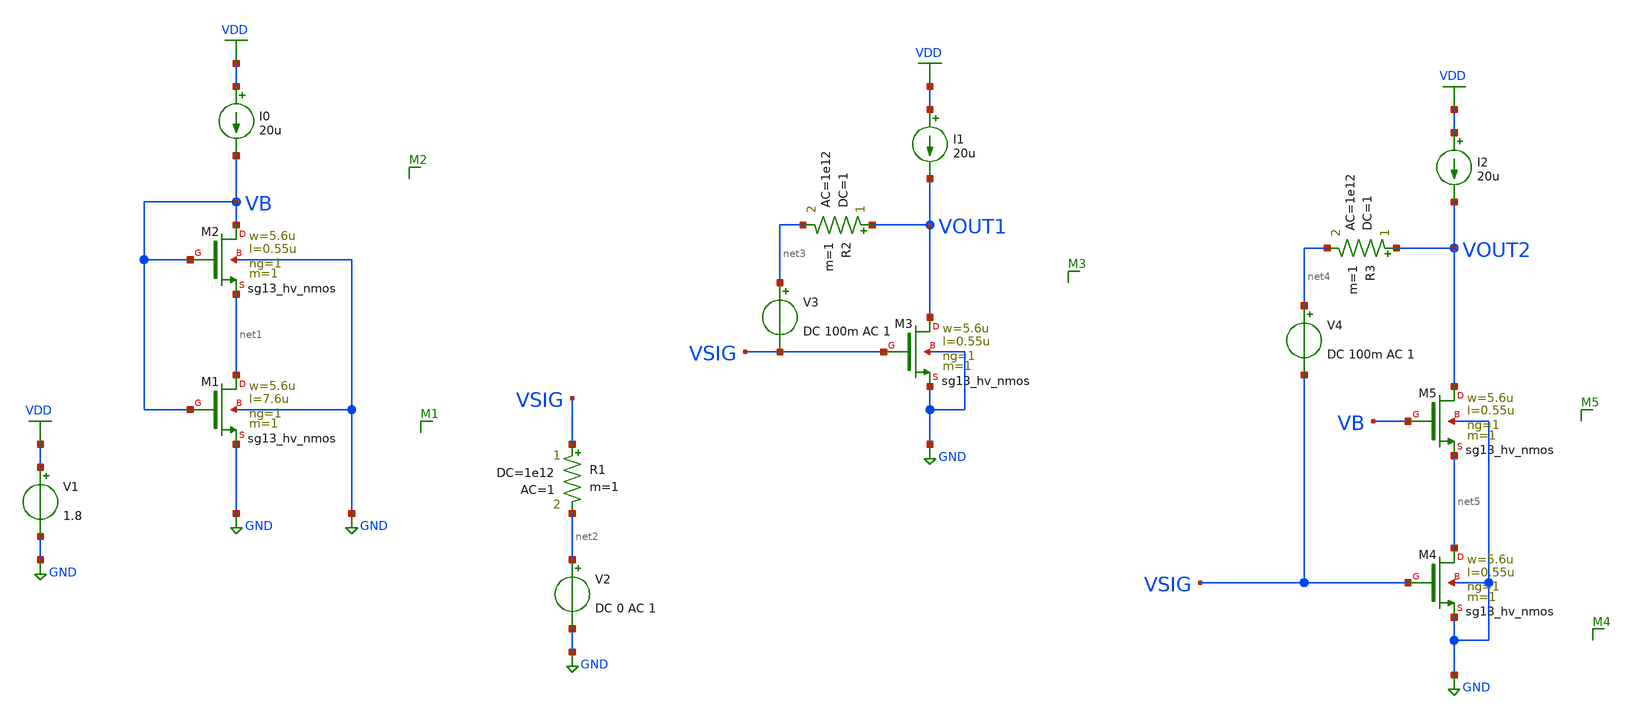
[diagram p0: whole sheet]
** sch_path: Schematics/lab_2/cascode_amplifier.sch
**.subckt cascode_amplifier
XM1 net1 VB GND GND sg13_hv_nmos w=5.6u l=7.6u ng=1 m=1 mm_ok=1
XM2 VB VB net1 GND sg13_hv_nmos w=5.6u l=0.55u ng=1 m=1 mm_ok=1
I0 VDD VB 20u
V1 VDD GND 1.8
XM3 VOUT1 VSIG GND GND sg13_hv_nmos w=5.6u l=0.55u ng=1 m=1 mm_ok=1
I1 VDD VOUT1 20u
V2 net2 GND DC 0 AC 1
R1 VSIG net2 1e12 ac=1 m=1
V3 net3 VSIG DC 100m AC 1
R2 VOUT1 net3 1 ac=1e12 m=1
XM4 net5 VSIG GND GND sg13_hv_nmos w=5.6u l=0.55u ng=1 m=1 mm_ok=1
I2 VDD VOUT2 20u
V4 net4 VSIG DC 100m AC 1
R3 VOUT2 net4 1 ac=1e12 m=1
XM5 VOUT2 VB net5 GND sg13_hv_nmos w=5.6u l=0.55u ng=1 m=1 mm_ok=1
**** begin user architecture code



.lib cornerMOSlv.lib mos_tt
.lib cornerMOShv.lib mos_tt
.lib cornerHBT.lib hbt_typ
.lib cornerRES.lib res_typ






.include cascode_amplifier.save
.control

alterparam sw_stat_global = 0
alterparam sw_stat_mismatch = 0
reset


save all
op
write cascode_amplifier.raw
set appendwrite

ac dec 10 1 10g

meas ac DC_gain_1 find vmag(VOUT1) at=1
let A3db= DC_gain_1 / sqrt(2)
meas ac BW_1 when vmag(VOUT1)=A3db fall=1
let GBW_1 = DC_gain_1 * BW_1
meas ac UGF_1 when vmag(VOUT1)=1 fall=1



meas ac DC_gain_2 find vmag(VOUT2) at=1
let A3db= DC_gain_2 / sqrt(2)
meas ac BW_2 when vmag(VOUT2)=A3db fall=1
let GBW_2 = DC_gain_2 * BW_2
meas ac UGF_2 when vmag(VOUT2)=1 fall=1

print DC_gain_1 BW_1 GBW_1 UGF_1 > lab_2_results.txt
print DC_gain_2 BW_2 GBW_2 UGF_2 >> lab_2_results.txt

remzerovec
write cascode_amplifier.raw


.endc



**** end user architecture code
**.ends
.GLOBAL GND
.GLOBAL VDD
.end
